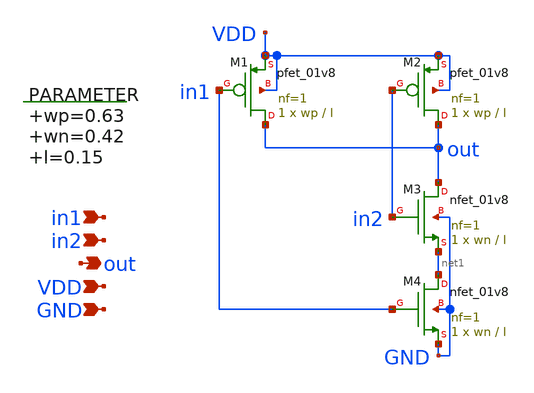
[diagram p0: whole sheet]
** sch_path: xschem/nand.sch
**.subckt nand in2 out VDD GND in1
*.ipin in2
*.opin out
*.ipin VDD
*.ipin GND
*.ipin in1
.param wp=0.63 wn=0.42 l=0.15
XM1 out in1 VDD VDD sky130_fd_pr__pfet_01v8 L=l W=wp nf=1 ad='int((nf+1)/2) * W/nf * 0.29' as='int((nf+2)/2) * W/nf * 0.29'
+ pd='2*int((nf+1)/2) * (W/nf + 0.29)' ps='2*int((nf+2)/2) * (W/nf + 0.29)' nrd='0.29 / W' nrs='0.29 / W'
+ sa=0 sb=0 sd=0 mult=1 m=1
XM2 out in2 VDD VDD sky130_fd_pr__pfet_01v8 L=l W=wp nf=1 ad='int((nf+1)/2) * W/nf * 0.29' as='int((nf+2)/2) * W/nf * 0.29'
+ pd='2*int((nf+1)/2) * (W/nf + 0.29)' ps='2*int((nf+2)/2) * (W/nf + 0.29)' nrd='0.29 / W' nrs='0.29 / W'
+ sa=0 sb=0 sd=0 mult=1 m=1
XM3 out in2 net1 GND sky130_fd_pr__nfet_01v8 L=l W=wn nf=1 ad='int((nf+1)/2) * W/nf * 0.29' as='int((nf+2)/2) * W/nf * 0.29'
+ pd='2*int((nf+1)/2) * (W/nf + 0.29)' ps='2*int((nf+2)/2) * (W/nf + 0.29)' nrd='0.29 / W' nrs='0.29 / W'
+ sa=0 sb=0 sd=0 mult=1 m=1
XM4 net1 in1 GND GND sky130_fd_pr__nfet_01v8 L=l W=wn nf=1 ad='int((nf+1)/2) * W/nf * 0.29' as='int((nf+2)/2) * W/nf * 0.29'
+ pd='2*int((nf+1)/2) * (W/nf + 0.29)' ps='2*int((nf+2)/2) * (W/nf + 0.29)' nrd='0.29 / W' nrs='0.29 / W'
+ sa=0 sb=0 sd=0 mult=1 m=1
**.ends
.end
